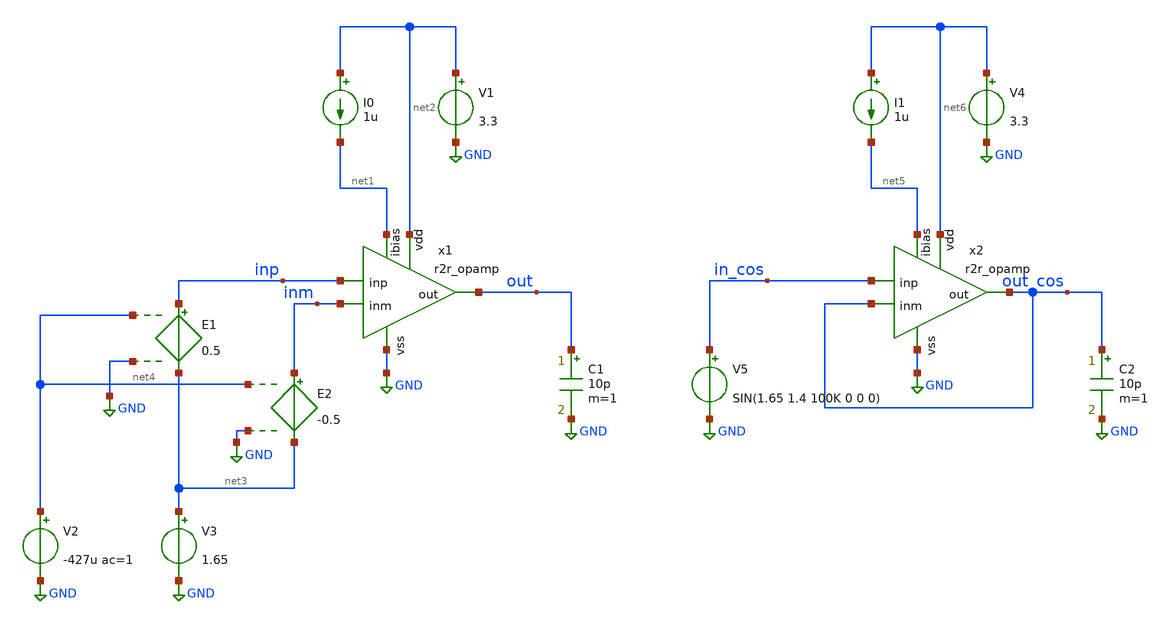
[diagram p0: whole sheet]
** sch_path: xschem/tb_r2r_opamp.sch
**.subckt tb_r2r_opamp
x1 net2 out net1 inp inm GND r2r_opamp
I0 net2 net1 1u
V1 net2 GND 3.3
V2 net4 GND -427u ac=1
V3 net3 GND 1.65
E1 inp net3 net4 GND 0.5
E2 inm net3 net4 GND -0.5
C1 out GND 10p m=1
x2 net6 out_cos net5 in_cos out_cos GND r2r_opamp
I1 net6 net5 1u
V4 net6 GND 3.3
C2 out_cos GND 10p m=1
V5 in_cos GND SIN(1.65 1.4 100K 0 0 0)
**** begin user architecture code


.include /usr/local/share/pdk/gf180mcuD/libs.tech/ngspice/design.ngspice
.lib /usr/local/share/pdk/gf180mcuD/libs.tech/ngspice/sm141064.ngspice ss
.option temp=110

.control
save all
dc V2 -0.2 0.2 10u
run
meas dc voffset WHEN v(out)=1.65 CROSS=1
echo Offset Voltage = $&voffset
plot v(out)
plot i(V1)

ac dec 100 1K 1G
run
plot db(v(out)) 180/PI*phase(v(out))

tran 1ns 100u
plot v(in_cos) v(out_cos)
.endc


**** end user architecture code
**.ends

* expanding   symbol:  r2r_opamp.sym # of pins=6
** sym_path: xschem/r2r_opamp.sym
** sch_path: xschem/r2r_opamp.sch
.subckt r2r_opamp vdd out ibias inp inm vss
*.ipin vss
*.ipin vdd
*.ipin ibias
*.ipin inp
*.ipin inm
*.opin out
XM1 net3 inp net8 vss nfet_03v3 L=0.28u W=16u nf=1 ad='int((nf+1)/2) * W/nf * 0.18u' as='int((nf+2)/2) * W/nf * 0.18u'
+ pd='2*int((nf+1)/2) * (W/nf + 0.18u)' ps='2*int((nf+2)/2) * (W/nf + 0.18u)' nrd='0.18u / W' nrs='0.18u / W'
+ sa=0 sb=0 sd=0 m=1
XM2 net4 inm net8 vss nfet_03v3 L=0.28u W=16u nf=1 ad='int((nf+1)/2) * W/nf * 0.18u' as='int((nf+2)/2) * W/nf * 0.18u'
+ pd='2*int((nf+1)/2) * (W/nf + 0.18u)' ps='2*int((nf+2)/2) * (W/nf + 0.18u)' nrd='0.18u / W' nrs='0.18u / W'
+ sa=0 sb=0 sd=0 m=1
XM3 net8 ibias vss vss nfet_03v3 L=0.5u W=16u nf=1 ad='int((nf+1)/2) * W/nf * 0.18u' as='int((nf+2)/2) * W/nf * 0.18u'
+ pd='2*int((nf+1)/2) * (W/nf + 0.18u)' ps='2*int((nf+2)/2) * (W/nf + 0.18u)' nrd='0.18u / W' nrs='0.18u / W'
+ sa=0 sb=0 sd=0 m=1
XM4 net6 inp net1 vdd pfet_03v3 L=0.28u W=32u nf=1 ad='int((nf+1)/2) * W/nf * 0.18u' as='int((nf+2)/2) * W/nf * 0.18u'
+ pd='2*int((nf+1)/2) * (W/nf + 0.18u)' ps='2*int((nf+2)/2) * (W/nf + 0.18u)' nrd='0.18u / W' nrs='0.18u / W'
+ sa=0 sb=0 sd=0 m=1
XM5 net7 inm net1 vdd pfet_03v3 L=0.28u W=32u nf=1 ad='int((nf+1)/2) * W/nf * 0.18u' as='int((nf+2)/2) * W/nf * 0.18u'
+ pd='2*int((nf+1)/2) * (W/nf + 0.18u)' ps='2*int((nf+2)/2) * (W/nf + 0.18u)' nrd='0.18u / W' nrs='0.18u / W'
+ sa=0 sb=0 sd=0 m=1
XM6 net1 net2 vdd vdd pfet_03v3 L=0.5u W=32u nf=1 ad='int((nf+1)/2) * W/nf * 0.18u' as='int((nf+2)/2) * W/nf * 0.18u'
+ pd='2*int((nf+1)/2) * (W/nf + 0.18u)' ps='2*int((nf+2)/2) * (W/nf + 0.18u)' nrd='0.18u / W' nrs='0.18u / W'
+ sa=0 sb=0 sd=0 m=1
XM7 net5 vbiasn net6 vss nfet_03v3 L=0.5u W=8u nf=1 ad='int((nf+1)/2) * W/nf * 0.18u' as='int((nf+2)/2) * W/nf * 0.18u'
+ pd='2*int((nf+1)/2) * (W/nf + 0.18u)' ps='2*int((nf+2)/2) * (W/nf + 0.18u)' nrd='0.18u / W' nrs='0.18u / W'
+ sa=0 sb=0 sd=0 m=1
XM8 out vbiasn net7 vss nfet_03v3 L=0.5u W=8u nf=1 ad='int((nf+1)/2) * W/nf * 0.18u' as='int((nf+2)/2) * W/nf * 0.18u'
+ pd='2*int((nf+1)/2) * (W/nf + 0.18u)' ps='2*int((nf+2)/2) * (W/nf + 0.18u)' nrd='0.18u / W' nrs='0.18u / W'
+ sa=0 sb=0 sd=0 m=1
XM9 net6 ibias vss vss nfet_03v3 L=0.5u W=16u nf=1 ad='int((nf+1)/2) * W/nf * 0.18u' as='int((nf+2)/2) * W/nf * 0.18u'
+ pd='2*int((nf+1)/2) * (W/nf + 0.18u)' ps='2*int((nf+2)/2) * (W/nf + 0.18u)' nrd='0.18u / W' nrs='0.18u / W'
+ sa=0 sb=0 sd=0 m=1
XM10 net7 ibias vss vss nfet_03v3 L=0.5u W=16u nf=1 ad='int((nf+1)/2) * W/nf * 0.18u' as='int((nf+2)/2) * W/nf * 0.18u'
+ pd='2*int((nf+1)/2) * (W/nf + 0.18u)' ps='2*int((nf+2)/2) * (W/nf + 0.18u)' nrd='0.18u / W' nrs='0.18u / W'
+ sa=0 sb=0 sd=0 m=1
XM11 net5 vbiasp net3 vdd pfet_03v3 L=0.5u W=16u nf=1 ad='int((nf+1)/2) * W/nf * 0.18u' as='int((nf+2)/2) * W/nf * 0.18u'
+ pd='2*int((nf+1)/2) * (W/nf + 0.18u)' ps='2*int((nf+2)/2) * (W/nf + 0.18u)' nrd='0.18u / W' nrs='0.18u / W'
+ sa=0 sb=0 sd=0 m=1
XM12 out vbiasp net4 vdd pfet_03v3 L=0.5u W=16u nf=1 ad='int((nf+1)/2) * W/nf * 0.18u' as='int((nf+2)/2) * W/nf * 0.18u'
+ pd='2*int((nf+1)/2) * (W/nf + 0.18u)' ps='2*int((nf+2)/2) * (W/nf + 0.18u)' nrd='0.18u / W' nrs='0.18u / W'
+ sa=0 sb=0 sd=0 m=1
XM13 net3 net5 vdd vdd pfet_03v3 L=0.5u W=32u nf=1 ad='int((nf+1)/2) * W/nf * 0.18u' as='int((nf+2)/2) * W/nf * 0.18u'
+ pd='2*int((nf+1)/2) * (W/nf + 0.18u)' ps='2*int((nf+2)/2) * (W/nf + 0.18u)' nrd='0.18u / W' nrs='0.18u / W'
+ sa=0 sb=0 sd=0 m=1
XM14 net4 net5 vdd vdd pfet_03v3 L=0.5u W=32u nf=1 ad='int((nf+1)/2) * W/nf * 0.18u' as='int((nf+2)/2) * W/nf * 0.18u'
+ pd='2*int((nf+1)/2) * (W/nf + 0.18u)' ps='2*int((nf+2)/2) * (W/nf + 0.18u)' nrd='0.18u / W' nrs='0.18u / W'
+ sa=0 sb=0 sd=0 m=1
XM15 ibias ibias vss vss nfet_03v3 L=0.5u W=2u nf=1 ad='int((nf+1)/2) * W/nf * 0.18u' as='int((nf+2)/2) * W/nf * 0.18u'
+ pd='2*int((nf+1)/2) * (W/nf + 0.18u)' ps='2*int((nf+2)/2) * (W/nf + 0.18u)' nrd='0.18u / W' nrs='0.18u / W'
+ sa=0 sb=0 sd=0 m=1
XM16 net2 ibias vss vss nfet_03v3 L=0.5u W=2u nf=1 ad='int((nf+1)/2) * W/nf * 0.18u' as='int((nf+2)/2) * W/nf * 0.18u'
+ pd='2*int((nf+1)/2) * (W/nf + 0.18u)' ps='2*int((nf+2)/2) * (W/nf + 0.18u)' nrd='0.18u / W' nrs='0.18u / W'
+ sa=0 sb=0 sd=0 m=1
XM17 net2 net2 vdd vdd pfet_03v3 L=0.5u W=4u nf=1 ad='int((nf+1)/2) * W/nf * 0.18u' as='int((nf+2)/2) * W/nf * 0.18u'
+ pd='2*int((nf+1)/2) * (W/nf + 0.18u)' ps='2*int((nf+2)/2) * (W/nf + 0.18u)' nrd='0.18u / W' nrs='0.18u / W'
+ sa=0 sb=0 sd=0 m=1
XM18 vbiasp ibias vss vss nfet_03v3 L=0.5u W=8u nf=1 ad='int((nf+1)/2) * W/nf * 0.18u' as='int((nf+2)/2) * W/nf * 0.18u'
+ pd='2*int((nf+1)/2) * (W/nf + 0.18u)' ps='2*int((nf+2)/2) * (W/nf + 0.18u)' nrd='0.18u / W' nrs='0.18u / W'
+ sa=0 sb=0 sd=0 m=1
XM19 vbiasp vbiasp vdd vdd pfet_03v3 L=0.5u W=4u nf=1 ad='int((nf+1)/2) * W/nf * 0.18u' as='int((nf+2)/2) * W/nf * 0.18u'
+ pd='2*int((nf+1)/2) * (W/nf + 0.18u)' ps='2*int((nf+2)/2) * (W/nf + 0.18u)' nrd='0.18u / W' nrs='0.18u / W'
+ sa=0 sb=0 sd=0 m=1
XM20 vbiasn net2 vdd vdd pfet_03v3 L=0.5u W=16u nf=1 ad='int((nf+1)/2) * W/nf * 0.18u' as='int((nf+2)/2) * W/nf * 0.18u'
+ pd='2*int((nf+1)/2) * (W/nf + 0.18u)' ps='2*int((nf+2)/2) * (W/nf + 0.18u)' nrd='0.18u / W' nrs='0.18u / W'
+ sa=0 sb=0 sd=0 m=1
XM21 vbiasn vbiasn vss vss nfet_03v3 L=0.5u W=2u nf=1 ad='int((nf+1)/2) * W/nf * 0.18u' as='int((nf+2)/2) * W/nf * 0.18u'
+ pd='2*int((nf+1)/2) * (W/nf + 0.18u)' ps='2*int((nf+2)/2) * (W/nf + 0.18u)' nrd='0.18u / W' nrs='0.18u / W'
+ sa=0 sb=0 sd=0 m=1
.ends

.GLOBAL GND
.end
